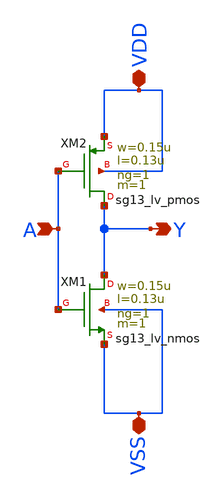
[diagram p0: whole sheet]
** sch_path: LogicGate/inverter.sch
**.subckt inverter A Y VDD VSS
*.ipin A
*.opin Y
*.iopin VDD
*.iopin VSS
XXM1 Y A VSS VSS sg13_lv_nmos w=0.15u l=0.13u ng=1 m=1 mm_ok=1
XXM2 Y A VDD VDD sg13_lv_pmos w=0.15u l=0.13u ng=1 m=1 mm_ok=1
**.ends
.end
